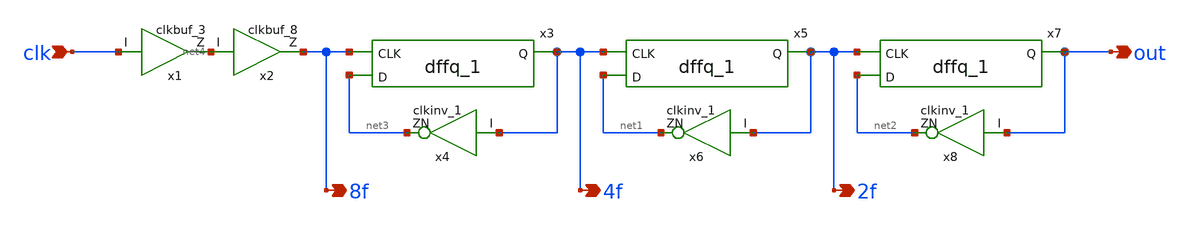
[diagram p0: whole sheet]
** sch_path: fdiv.sch
**.subckt fdiv clk out 2f 4f 8f
*.ipin clk
*.opin out
*.opin 2f
*.opin 4f
*.opin 8f
x5 net1 4f 2f VDD VDD GND GND gf180mcu_fd_sc_mcu7t5v0__dffq_1
x6 2f net1 VDD VDD GND GND gf180mcu_fd_sc_mcu7t5v0__clkinv_1
x1 clk net4 VDD VDD GND GND gf180mcu_fd_sc_mcu7t5v0__clkbuf_3
x2 net4 8f VDD VDD GND GND gf180mcu_fd_sc_mcu7t5v0__clkbuf_8
x3 net3 8f 4f VDD VDD GND GND gf180mcu_fd_sc_mcu7t5v0__dffq_1
x4 4f net3 VDD VDD GND GND gf180mcu_fd_sc_mcu7t5v0__clkinv_1
x7 net2 2f out VDD VDD GND GND gf180mcu_fd_sc_mcu7t5v0__dffq_1
x8 out net2 VDD VDD GND GND gf180mcu_fd_sc_mcu7t5v0__clkinv_1
**.ends
.end
